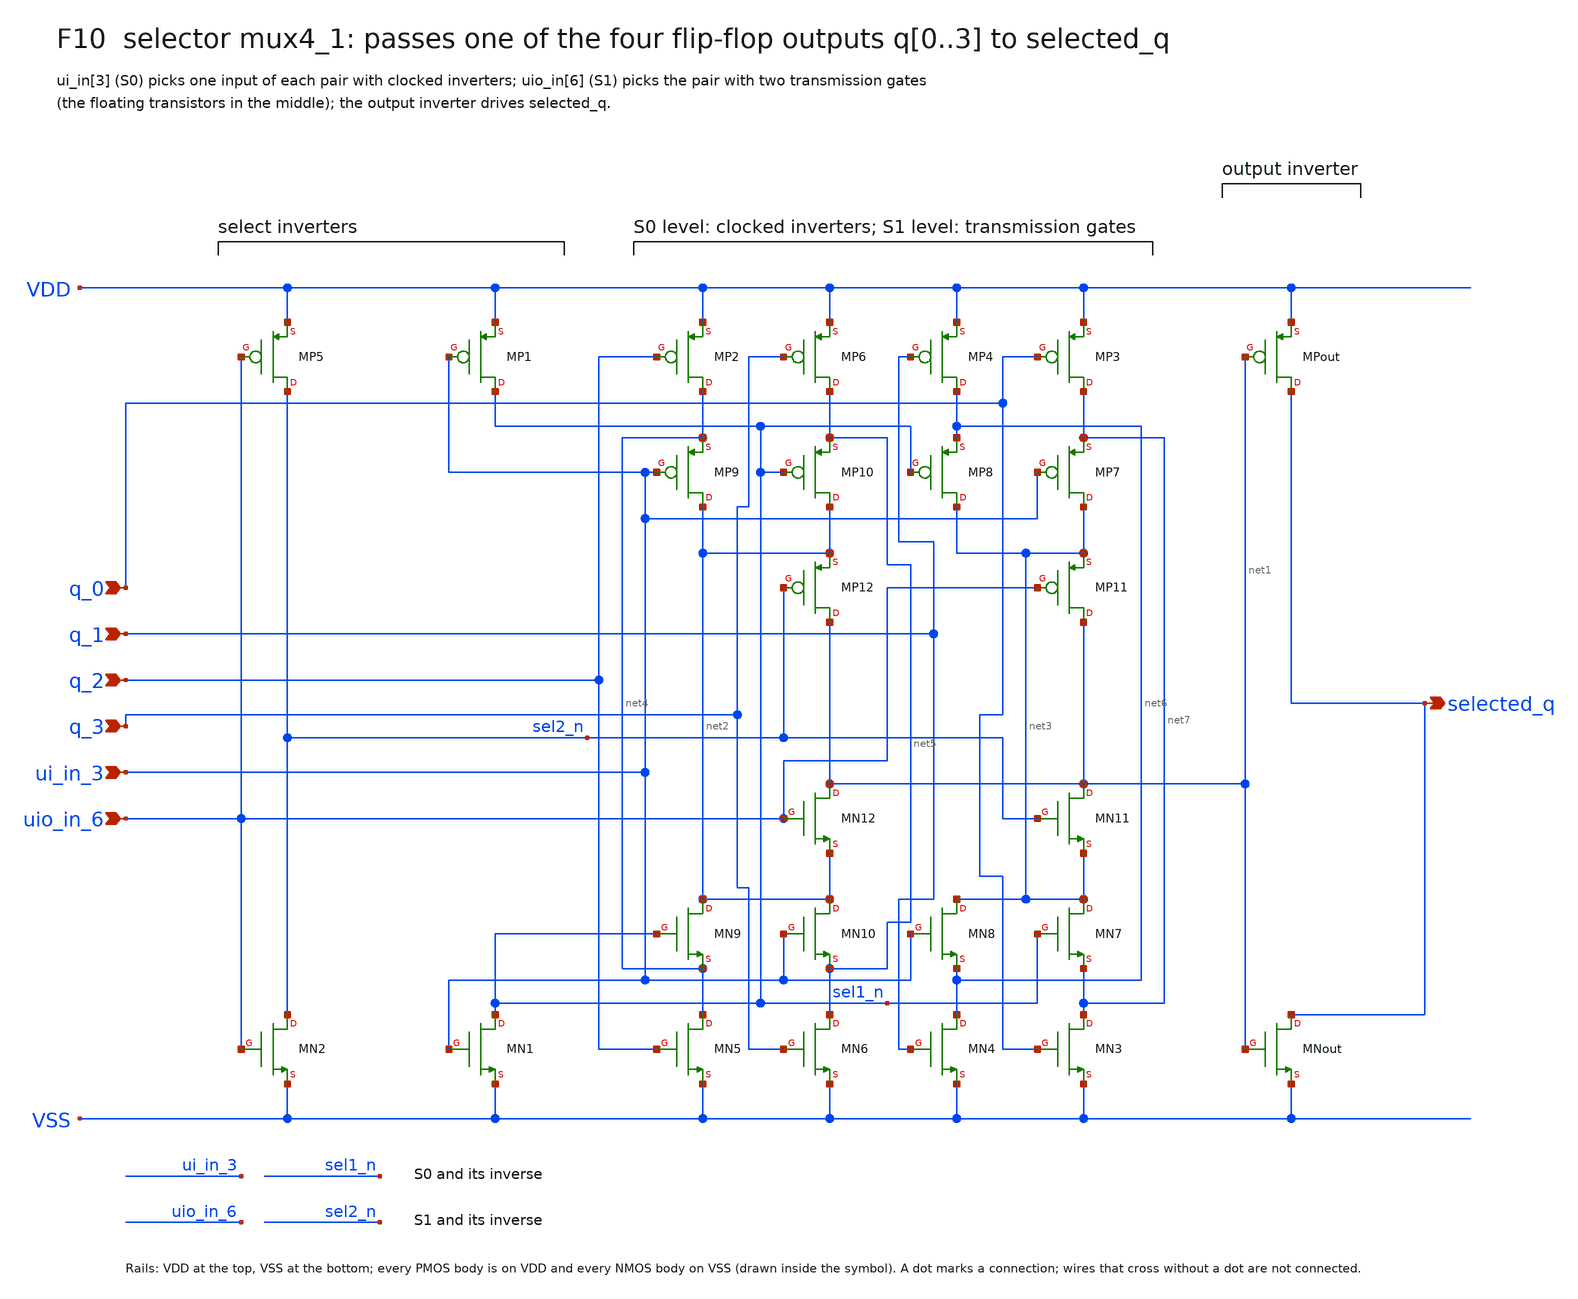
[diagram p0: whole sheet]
** sch_path: xschem/focus/F10_selector.sch
**.subckt F10_selector q_0 q_1 q_2 q_3 ui_in_3 uio_in_6 selected_q
*.ipin q_0
*.ipin q_1
*.ipin q_2
*.ipin q_3
*.ipin ui_in_3
*.ipin uio_in_6
*.opin selected_q
XMN5 net4 q_2 VSS VSS nfet_05v0 L=0.6u W=0.365u nf=1 m=1
XMN9 net2 sel1_n net4 VSS nfet_05v0 L=0.6u W=0.365u nf=1 m=1
XMN10 net2 ui_in_3 net5 VSS nfet_05v0 L=0.6u W=0.365u nf=1 m=1
XMN6 net5 q_3 VSS VSS nfet_05v0 L=0.6u W=0.365u nf=1 m=1
XMNout selected_q net1 VSS VSS nfet_05v0 L=0.6u W=0.38u nf=1 m=1
XMN12 net1 uio_in_6 net2 VSS nfet_05v0 L=0.6u W=0.365u nf=1 m=1
XMN11 net1 sel2_n net3 VSS nfet_05v0 L=0.6u W=0.365u nf=1 m=1
XMN2 sel2_n uio_in_6 VSS VSS nfet_05v0 L=0.6u W=0.365u nf=1 m=1
XMN4 net6 q_1 VSS VSS nfet_05v0 L=0.6u W=0.365u nf=1 m=1
XMN8 net3 ui_in_3 net6 VSS nfet_05v0 L=0.6u W=0.365u nf=1 m=1
XMN7 net3 sel1_n net7 VSS nfet_05v0 L=0.6u W=0.365u nf=1 m=1
XMN3 net7 q_0 VSS VSS nfet_05v0 L=0.6u W=0.365u nf=1 m=1
XMN1 sel1_n ui_in_3 VSS VSS nfet_05v0 L=0.6u W=0.365u nf=1 m=1
XMP2 net4 q_2 VDD VDD pfet_05v0 L=0.5u W=0.565u nf=1 m=1
XMP9 net2 ui_in_3 net4 VDD pfet_05v0 L=0.5u W=0.565u nf=1 m=1
XMP10 net2 sel1_n net5 VDD pfet_05v0 L=0.5u W=0.565u nf=1 m=1
XMP6 net5 q_3 VDD VDD pfet_05v0 L=0.5u W=0.565u nf=1 m=1
XMPout selected_q net1 VDD VDD pfet_05v0 L=0.5u W=0.78u nf=1 m=1
XMP12 net1 sel2_n net2 VDD pfet_05v0 L=0.5u W=0.565u nf=1 m=1
XMP11 net1 uio_in_6 net3 VDD pfet_05v0 L=0.5u W=0.565u nf=1 m=1
XMP5 sel2_n uio_in_6 VDD VDD pfet_05v0 L=0.5u W=0.565u nf=1 m=1
XMP4 net6 q_1 VDD VDD pfet_05v0 L=0.5u W=0.565u nf=1 m=1
XMP8 net3 sel1_n net6 VDD pfet_05v0 L=0.5u W=0.565u nf=1 m=1
XMP7 net3 ui_in_3 net7 VDD pfet_05v0 L=0.5u W=0.565u nf=1 m=1
XMP3 net7 q_0 VDD VDD pfet_05v0 L=0.5u W=0.565u nf=1 m=1
XMP1 sel1_n ui_in_3 VDD VDD pfet_05v0 L=0.5u W=0.565u nf=1 m=1
**.ends
.end
